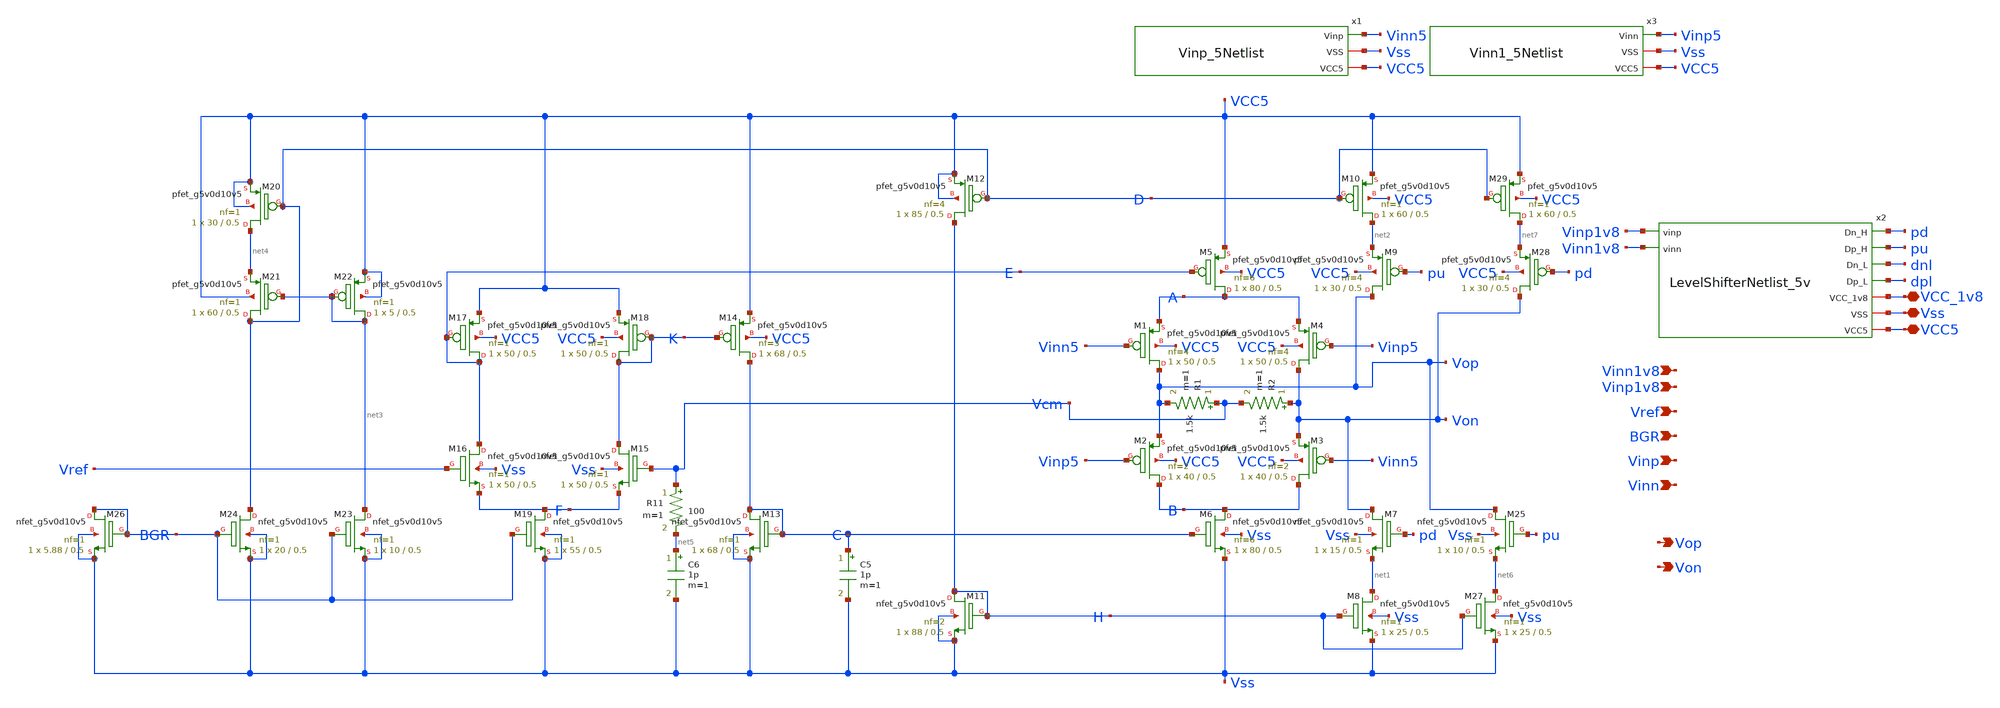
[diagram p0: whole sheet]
** sch_path: Git Files/Schematic/OutputDriverNetlist_5v.sch
**.subckt OutputDriverNetlist_5v Vinp Vinn Vop Von VCC5 Vss VCC_1v8 BGR Vref Vinp1v8 Vinn1v8
*.ipin Vinp
*.ipin Vinn
*.opin Vop
*.opin Von
*.iopin VCC5
*.iopin Vss
*.iopin VCC_1v8
*.ipin BGR
*.ipin Vref
*.ipin Vinp1v8
*.ipin Vinn1v8
R1 Vcm Vop 1.5k m=1
R2 Von Vcm 1.5k m=1
C5 C Vss 1p m=1
C6 net5 Vss 1p m=1
R11 Vcm net5 100 m=1
XM27 net6 H Vss Vss sky130_fd_pr__nfet_g5v0d10v5 L=0.5 W=25 nf=1 ad='int((nf+1)/2) * W/nf * 0.29' as='int((nf+2)/2) * W/nf * 0.29'
+ pd='2*int((nf+1)/2) * (W/nf + 0.29)' ps='2*int((nf+2)/2) * (W/nf + 0.29)' nrd='0.29 / W' nrs='0.29 / W'
+ sa=0 sb=0 sd=0 mult=1 m=1
XM8 net1 H Vss Vss sky130_fd_pr__nfet_g5v0d10v5 L=0.5 W=25 nf=1 ad='int((nf+1)/2) * W/nf * 0.29' as='int((nf+2)/2) * W/nf * 0.29'
+ pd='2*int((nf+1)/2) * (W/nf + 0.29)' ps='2*int((nf+2)/2) * (W/nf + 0.29)' nrd='0.29 / W' nrs='0.29 / W'
+ sa=0 sb=0 sd=0 mult=1 m=1
XM25 Vop pu net6 Vss sky130_fd_pr__nfet_g5v0d10v5 L=0.5 W=10 nf=1 ad='int((nf+1)/2) * W/nf * 0.29' as='int((nf+2)/2) * W/nf * 0.29'
+ pd='2*int((nf+1)/2) * (W/nf + 0.29)' ps='2*int((nf+2)/2) * (W/nf + 0.29)' nrd='0.29 / W' nrs='0.29 / W'
+ sa=0 sb=0 sd=0 mult=1 m=1
XM7 Von pd net1 Vss sky130_fd_pr__nfet_g5v0d10v5 L=0.5 W=15 nf=1 ad='int((nf+1)/2) * W/nf * 0.29' as='int((nf+2)/2) * W/nf * 0.29'
+ pd='2*int((nf+1)/2) * (W/nf + 0.29)' ps='2*int((nf+2)/2) * (W/nf + 0.29)' nrd='0.29 / W' nrs='0.29 / W'
+ sa=0 sb=0 sd=0 mult=1 m=1
XM6 B C Vss Vss sky130_fd_pr__nfet_g5v0d10v5 L=0.5 W=80 nf=6 ad='int((nf+1)/2) * W/nf * 0.29' as='int((nf+2)/2) * W/nf * 0.29'
+ pd='2*int((nf+1)/2) * (W/nf + 0.29)' ps='2*int((nf+2)/2) * (W/nf + 0.29)' nrd='0.29 / W' nrs='0.29 / W'
+ sa=0 sb=0 sd=0 mult=1 m=1
XM11 H H Vss Vss sky130_fd_pr__nfet_g5v0d10v5 L=0.5 W=88 nf=2 ad='int((nf+1)/2) * W/nf * 0.29' as='int((nf+2)/2) * W/nf * 0.29'
+ pd='2*int((nf+1)/2) * (W/nf + 0.29)' ps='2*int((nf+2)/2) * (W/nf + 0.29)' nrd='0.29 / W' nrs='0.29 / W'
+ sa=0 sb=0 sd=0 mult=1 m=1
XM13 C C Vss Vss sky130_fd_pr__nfet_g5v0d10v5 L=0.5 W=68 nf=1 ad='int((nf+1)/2) * W/nf * 0.29' as='int((nf+2)/2) * W/nf * 0.29'
+ pd='2*int((nf+1)/2) * (W/nf + 0.29)' ps='2*int((nf+2)/2) * (W/nf + 0.29)' nrd='0.29 / W' nrs='0.29 / W'
+ sa=0 sb=0 sd=0 mult=1 m=1
XM15 K Vcm F Vss sky130_fd_pr__nfet_g5v0d10v5 L=0.5 W=50 nf=1 ad='int((nf+1)/2) * W/nf * 0.29' as='int((nf+2)/2) * W/nf * 0.29'
+ pd='2*int((nf+1)/2) * (W/nf + 0.29)' ps='2*int((nf+2)/2) * (W/nf + 0.29)' nrd='0.29 / W' nrs='0.29 / W'
+ sa=0 sb=0 sd=0 mult=1 m=1
XM19 F BGR Vss Vss sky130_fd_pr__nfet_g5v0d10v5 L=0.5 W=55 nf=1 ad='int((nf+1)/2) * W/nf * 0.29' as='int((nf+2)/2) * W/nf * 0.29'
+ pd='2*int((nf+1)/2) * (W/nf + 0.29)' ps='2*int((nf+2)/2) * (W/nf + 0.29)' nrd='0.29 / W' nrs='0.29 / W'
+ sa=0 sb=0 sd=0 mult=1 m=1
XM16 E Vref F Vss sky130_fd_pr__nfet_g5v0d10v5 L=0.5 W=50 nf=1 ad='int((nf+1)/2) * W/nf * 0.29' as='int((nf+2)/2) * W/nf * 0.29'
+ pd='2*int((nf+1)/2) * (W/nf + 0.29)' ps='2*int((nf+2)/2) * (W/nf + 0.29)' nrd='0.29 / W' nrs='0.29 / W'
+ sa=0 sb=0 sd=0 mult=1 m=1
XM23 net3 BGR Vss Vss sky130_fd_pr__nfet_g5v0d10v5 L=0.5 W=10 nf=1 ad='int((nf+1)/2) * W/nf * 0.29' as='int((nf+2)/2) * W/nf * 0.29'
+ pd='2*int((nf+1)/2) * (W/nf + 0.29)' ps='2*int((nf+2)/2) * (W/nf + 0.29)' nrd='0.29 / W' nrs='0.29 / W'
+ sa=0 sb=0 sd=0 mult=1 m=1
XM24 D BGR Vss Vss sky130_fd_pr__nfet_g5v0d10v5 L=0.5 W=20 nf=1 ad='int((nf+1)/2) * W/nf * 0.29' as='int((nf+2)/2) * W/nf * 0.29'
+ pd='2*int((nf+1)/2) * (W/nf + 0.29)' ps='2*int((nf+2)/2) * (W/nf + 0.29)' nrd='0.29 / W' nrs='0.29 / W'
+ sa=0 sb=0 sd=0 mult=1 m=1
XM26 BGR BGR Vss Vss sky130_fd_pr__nfet_g5v0d10v5 L=0.5 W=5.88 nf=1 ad='int((nf+1)/2) * W/nf * 0.29'
+ as='int((nf+2)/2) * W/nf * 0.29' pd='2*int((nf+1)/2) * (W/nf + 0.29)' ps='2*int((nf+2)/2) * (W/nf + 0.29)'
+ nrd='0.29 / W' nrs='0.29 / W' sa=0 sb=0 sd=0 mult=1 m=1
XM21 D net3 net4 VCC5 sky130_fd_pr__pfet_g5v0d10v5 L=0.5 W=60 nf=1 ad='int((nf+1)/2) * W/nf * 0.29' as='int((nf+2)/2) * W/nf * 0.29'
+ pd='2*int((nf+1)/2) * (W/nf + 0.29)' ps='2*int((nf+2)/2) * (W/nf + 0.29)' nrd='0.29 / W' nrs='0.29 / W'
+ sa=0 sb=0 sd=0 mult=1 m=1
XM20 net4 D VCC5 VCC5 sky130_fd_pr__pfet_g5v0d10v5 L=0.5 W=30 nf=1 ad='int((nf+1)/2) * W/nf * 0.29' as='int((nf+2)/2) * W/nf * 0.29'
+ pd='2*int((nf+1)/2) * (W/nf + 0.29)' ps='2*int((nf+2)/2) * (W/nf + 0.29)' nrd='0.29 / W' nrs='0.29 / W'
+ sa=0 sb=0 sd=0 mult=1 m=1
XM22 net3 net3 VCC5 VCC5 sky130_fd_pr__pfet_g5v0d10v5 L=0.5 W=5 nf=1 ad='int((nf+1)/2) * W/nf * 0.29'
+ as='int((nf+2)/2) * W/nf * 0.29' pd='2*int((nf+1)/2) * (W/nf + 0.29)' ps='2*int((nf+2)/2) * (W/nf + 0.29)'
+ nrd='0.29 / W' nrs='0.29 / W' sa=0 sb=0 sd=0 mult=1 m=1
XM17 E E VCC5 VCC5 sky130_fd_pr__pfet_g5v0d10v5 L=0.5 W=50 nf=1 ad='int((nf+1)/2) * W/nf * 0.29' as='int((nf+2)/2) * W/nf * 0.29'
+ pd='2*int((nf+1)/2) * (W/nf + 0.29)' ps='2*int((nf+2)/2) * (W/nf + 0.29)' nrd='0.29 / W' nrs='0.29 / W'
+ sa=0 sb=0 sd=0 mult=1 m=1
XM18 K K VCC5 VCC5 sky130_fd_pr__pfet_g5v0d10v5 L=0.5 W=50 nf=1 ad='int((nf+1)/2) * W/nf * 0.29' as='int((nf+2)/2) * W/nf * 0.29'
+ pd='2*int((nf+1)/2) * (W/nf + 0.29)' ps='2*int((nf+2)/2) * (W/nf + 0.29)' nrd='0.29 / W' nrs='0.29 / W'
+ sa=0 sb=0 sd=0 mult=1 m=1
XM14 C K VCC5 VCC5 sky130_fd_pr__pfet_g5v0d10v5 L=0.5 W=68 nf=3 ad='int((nf+1)/2) * W/nf * 0.29' as='int((nf+2)/2) * W/nf * 0.29'
+ pd='2*int((nf+1)/2) * (W/nf + 0.29)' ps='2*int((nf+2)/2) * (W/nf + 0.29)' nrd='0.29 / W' nrs='0.29 / W'
+ sa=0 sb=0 sd=0 mult=1 m=1
XM12 H D VCC5 VCC5 sky130_fd_pr__pfet_g5v0d10v5 L=0.5 W=85 nf=4 ad='int((nf+1)/2) * W/nf * 0.29' as='int((nf+2)/2) * W/nf * 0.29'
+ pd='2*int((nf+1)/2) * (W/nf + 0.29)' ps='2*int((nf+2)/2) * (W/nf + 0.29)' nrd='0.29 / W' nrs='0.29 / W'
+ sa=0 sb=0 sd=0 mult=1 m=1
XM1 Vop Vinn5 A VCC5 sky130_fd_pr__pfet_g5v0d10v5 L=0.5 W=50 nf=4 ad='int((nf+1)/2) * W/nf * 0.29' as='int((nf+2)/2) * W/nf * 0.29'
+ pd='2*int((nf+1)/2) * (W/nf + 0.29)' ps='2*int((nf+2)/2) * (W/nf + 0.29)' nrd='0.29 / W' nrs='0.29 / W'
+ sa=0 sb=0 sd=0 mult=1 m=1
XM4 Von Vinp5 A VCC5 sky130_fd_pr__pfet_g5v0d10v5 L=0.5 W=50 nf=4 ad='int((nf+1)/2) * W/nf * 0.29' as='int((nf+2)/2) * W/nf * 0.29'
+ pd='2*int((nf+1)/2) * (W/nf + 0.29)' ps='2*int((nf+2)/2) * (W/nf + 0.29)' nrd='0.29 / W' nrs='0.29 / W'
+ sa=0 sb=0 sd=0 mult=1 m=1
XM3 B Vinn5 Von VCC5 sky130_fd_pr__pfet_g5v0d10v5 L=0.5 W=40 nf=2 ad='int((nf+1)/2) * W/nf * 0.29' as='int((nf+2)/2) * W/nf * 0.29'
+ pd='2*int((nf+1)/2) * (W/nf + 0.29)' ps='2*int((nf+2)/2) * (W/nf + 0.29)' nrd='0.29 / W' nrs='0.29 / W'
+ sa=0 sb=0 sd=0 mult=1 m=1
XM2 B Vinp5 Vop VCC5 sky130_fd_pr__pfet_g5v0d10v5 L=0.5 W=40 nf=2 ad='int((nf+1)/2) * W/nf * 0.29' as='int((nf+2)/2) * W/nf * 0.29'
+ pd='2*int((nf+1)/2) * (W/nf + 0.29)' ps='2*int((nf+2)/2) * (W/nf + 0.29)' nrd='0.29 / W' nrs='0.29 / W'
+ sa=0 sb=0 sd=0 mult=1 m=1
XM5 A E VCC5 VCC5 sky130_fd_pr__pfet_g5v0d10v5 L=0.5 W=80 nf=6 ad='int((nf+1)/2) * W/nf * 0.29' as='int((nf+2)/2) * W/nf * 0.29'
+ pd='2*int((nf+1)/2) * (W/nf + 0.29)' ps='2*int((nf+2)/2) * (W/nf + 0.29)' nrd='0.29 / W' nrs='0.29 / W'
+ sa=0 sb=0 sd=0 mult=1 m=1
XM10 net2 D VCC5 VCC5 sky130_fd_pr__pfet_g5v0d10v5 L=0.5 W=60 nf=1 ad='int((nf+1)/2) * W/nf * 0.29' as='int((nf+2)/2) * W/nf * 0.29'
+ pd='2*int((nf+1)/2) * (W/nf + 0.29)' ps='2*int((nf+2)/2) * (W/nf + 0.29)' nrd='0.29 / W' nrs='0.29 / W'
+ sa=0 sb=0 sd=0 mult=1 m=1
XM9 Vop pu net2 VCC5 sky130_fd_pr__pfet_g5v0d10v5 L=0.5 W=30 nf=4 ad='int((nf+1)/2) * W/nf * 0.29' as='int((nf+2)/2) * W/nf * 0.29'
+ pd='2*int((nf+1)/2) * (W/nf + 0.29)' ps='2*int((nf+2)/2) * (W/nf + 0.29)' nrd='0.29 / W' nrs='0.29 / W'
+ sa=0 sb=0 sd=0 mult=1 m=1
XM28 Von pd net7 VCC5 sky130_fd_pr__pfet_g5v0d10v5 L=0.5 W=30 nf=4 ad='int((nf+1)/2) * W/nf * 0.29' as='int((nf+2)/2) * W/nf * 0.29'
+ pd='2*int((nf+1)/2) * (W/nf + 0.29)' ps='2*int((nf+2)/2) * (W/nf + 0.29)' nrd='0.29 / W' nrs='0.29 / W'
+ sa=0 sb=0 sd=0 mult=1 m=1
XM29 net7 D VCC5 VCC5 sky130_fd_pr__pfet_g5v0d10v5 L=0.5 W=60 nf=1 ad='int((nf+1)/2) * W/nf * 0.29' as='int((nf+2)/2) * W/nf * 0.29'
+ pd='2*int((nf+1)/2) * (W/nf + 0.29)' ps='2*int((nf+2)/2) * (W/nf + 0.29)' nrd='0.29 / W' nrs='0.29 / W'
+ sa=0 sb=0 sd=0 mult=1 m=1
x2 pd pu dnl dpl Vinp1v8 Vinn1v8 VCC_1v8 Vss VCC5 LevelShifterNetlist_5v
x3 Vinp5 Vss VCC5 Vinn1_5Netlist
x1 Vinn5 Vss VCC5 Vinp_5Netlist
**.ends
.end
